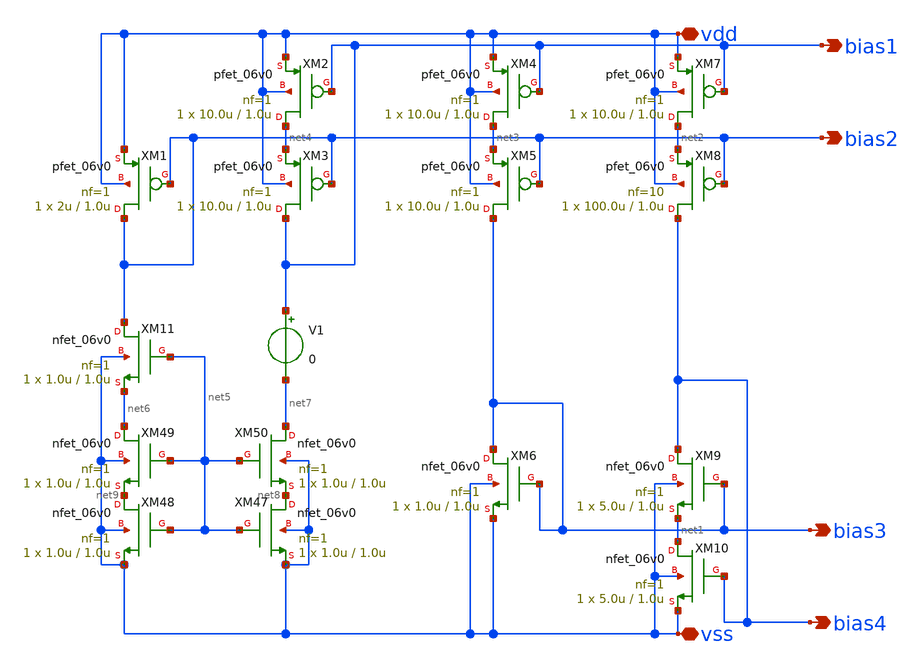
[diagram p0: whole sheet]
** sch_path: activities/opamp2AKAM/simulations_testbench/simulations_testbench/juanBias.sch
**.subckt juanBias bias1 bias2 bias3 bias4 vdd vss
*.opin bias1
*.opin bias2
*.opin bias3
*.opin bias4
*.iopin vdd
*.iopin vss
XM4 net3 bias1 vdd vdd pfet_06v0 L=1.0u W=10.0u nf=1 ad='int((nf+1)/2) * W/nf * 0.18u' as='int((nf+2)/2) * W/nf * 0.18u'
+ pd='2*int((nf+1)/2) * (W/nf + 0.18u)' ps='2*int((nf+2)/2) * (W/nf + 0.18u)' nrd='0.18u / W' nrs='0.18u / W'
+ sa=0 sb=0 sd=0 m=1
XM5 bias3 bias2 net3 vdd pfet_06v0 L=1.0u W=10.0u nf=1 ad='int((nf+1)/2) * W/nf * 0.18u' as='int((nf+2)/2) * W/nf * 0.18u'
+ pd='2*int((nf+1)/2) * (W/nf + 0.18u)' ps='2*int((nf+2)/2) * (W/nf + 0.18u)' nrd='0.18u / W' nrs='0.18u / W'
+ sa=0 sb=0 sd=0 m=1
XM6 bias3 bias3 vss vss nfet_06v0 L=1.0u W=1.0u nf=1 ad='int((nf+1)/2) * W/nf * 0.18u' as='int((nf+2)/2) * W/nf * 0.18u'
+ pd='2*int((nf+1)/2) * (W/nf + 0.18u)' ps='2*int((nf+2)/2) * (W/nf + 0.18u)' nrd='0.18u / W' nrs='0.18u / W'
+ sa=0 sb=0 sd=0 m=1
XM7 net2 bias1 vdd vdd pfet_06v0 L=1.0u W=10.0u nf=1 ad='int((nf+1)/2) * W/nf * 0.18u' as='int((nf+2)/2) * W/nf * 0.18u'
+ pd='2*int((nf+1)/2) * (W/nf + 0.18u)' ps='2*int((nf+2)/2) * (W/nf + 0.18u)' nrd='0.18u / W' nrs='0.18u / W'
+ sa=0 sb=0 sd=0 m=1
XM8 bias4 bias2 net2 vdd pfet_06v0 L=1.0u W=100.0u nf=10 ad='int((nf+1)/2) * W/nf * 0.18u' as='int((nf+2)/2) * W/nf * 0.18u'
+ pd='2*int((nf+1)/2) * (W/nf + 0.18u)' ps='2*int((nf+2)/2) * (W/nf + 0.18u)' nrd='0.18u / W' nrs='0.18u / W'
+ sa=0 sb=0 sd=0 m=1
XM9 bias4 bias3 net1 vss nfet_06v0 L=1.0u W=5.0u nf=1 ad='int((nf+1)/2) * W/nf * 0.18u' as='int((nf+2)/2) * W/nf * 0.18u'
+ pd='2*int((nf+1)/2) * (W/nf + 0.18u)' ps='2*int((nf+2)/2) * (W/nf + 0.18u)' nrd='0.18u / W' nrs='0.18u / W'
+ sa=0 sb=0 sd=0 m=1
XM10 net1 bias4 vss vss nfet_06v0 L=1.0u W=5.0u nf=1 ad='int((nf+1)/2) * W/nf * 0.18u' as='int((nf+2)/2) * W/nf * 0.18u'
+ pd='2*int((nf+1)/2) * (W/nf + 0.18u)' ps='2*int((nf+2)/2) * (W/nf + 0.18u)' nrd='0.18u / W' nrs='0.18u / W'
+ sa=0 sb=0 sd=0 m=1
XM1 bias2 bias2 vdd vdd pfet_06v0 L=1.0u W=2u nf=1 ad='int((nf+1)/2) * W/nf * 0.18u' as='int((nf+2)/2) * W/nf * 0.18u'
+ pd='2*int((nf+1)/2) * (W/nf + 0.18u)' ps='2*int((nf+2)/2) * (W/nf + 0.18u)' nrd='0.18u / W' nrs='0.18u / W'
+ sa=0 sb=0 sd=0 m=1
XM2 net4 bias1 vdd vdd pfet_06v0 L=1.0u W=10.0u nf=1 ad='int((nf+1)/2) * W/nf * 0.18u' as='int((nf+2)/2) * W/nf * 0.18u'
+ pd='2*int((nf+1)/2) * (W/nf + 0.18u)' ps='2*int((nf+2)/2) * (W/nf + 0.18u)' nrd='0.18u / W' nrs='0.18u / W'
+ sa=0 sb=0 sd=0 m=1
XM3 bias1 bias2 net4 vdd pfet_06v0 L=1.0u W=10.0u nf=1 ad='int((nf+1)/2) * W/nf * 0.18u' as='int((nf+2)/2) * W/nf * 0.18u'
+ pd='2*int((nf+1)/2) * (W/nf + 0.18u)' ps='2*int((nf+2)/2) * (W/nf + 0.18u)' nrd='0.18u / W' nrs='0.18u / W'
+ sa=0 sb=0 sd=0 m=1
XM47 net8 net5 vss vss nfet_06v0 L=1.0u W=1.0u nf=1 ad='int((nf+1)/2) * W/nf * 0.18u' as='int((nf+2)/2) * W/nf * 0.18u'
+ pd='2*int((nf+1)/2) * (W/nf + 0.18u)' ps='2*int((nf+2)/2) * (W/nf + 0.18u)' nrd='0.18u / W' nrs='0.18u / W'
+ sa=0 sb=0 sd=0 m=1
XM48 net9 net5 vss vss nfet_06v0 L=1.0u W=1.0u nf=1 ad='int((nf+1)/2) * W/nf * 0.18u' as='int((nf+2)/2) * W/nf * 0.18u'
+ pd='2*int((nf+1)/2) * (W/nf + 0.18u)' ps='2*int((nf+2)/2) * (W/nf + 0.18u)' nrd='0.18u / W' nrs='0.18u / W'
+ sa=0 sb=0 sd=0 m=1
XM49 net6 net5 net9 vss nfet_06v0 L=1.0u W=1.0u nf=1 ad='int((nf+1)/2) * W/nf * 0.18u' as='int((nf+2)/2) * W/nf * 0.18u'
+ pd='2*int((nf+1)/2) * (W/nf + 0.18u)' ps='2*int((nf+2)/2) * (W/nf + 0.18u)' nrd='0.18u / W' nrs='0.18u / W'
+ sa=0 sb=0 sd=0 m=1
XM50 net7 net5 net8 vss nfet_06v0 L=1.0u W=1.0u nf=1 ad='int((nf+1)/2) * W/nf * 0.18u' as='int((nf+2)/2) * W/nf * 0.18u'
+ pd='2*int((nf+1)/2) * (W/nf + 0.18u)' ps='2*int((nf+2)/2) * (W/nf + 0.18u)' nrd='0.18u / W' nrs='0.18u / W'
+ sa=0 sb=0 sd=0 m=1
XM11 bias2 net5 net6 vss nfet_06v0 L=1.0u W=1.0u nf=1 ad='int((nf+1)/2) * W/nf * 0.18u' as='int((nf+2)/2) * W/nf * 0.18u'
+ pd='2*int((nf+1)/2) * (W/nf + 0.18u)' ps='2*int((nf+2)/2) * (W/nf + 0.18u)' nrd='0.18u / W' nrs='0.18u / W'
+ sa=0 sb=0 sd=0 m=1
V1 bias1 net7 0
**.ends
.end
